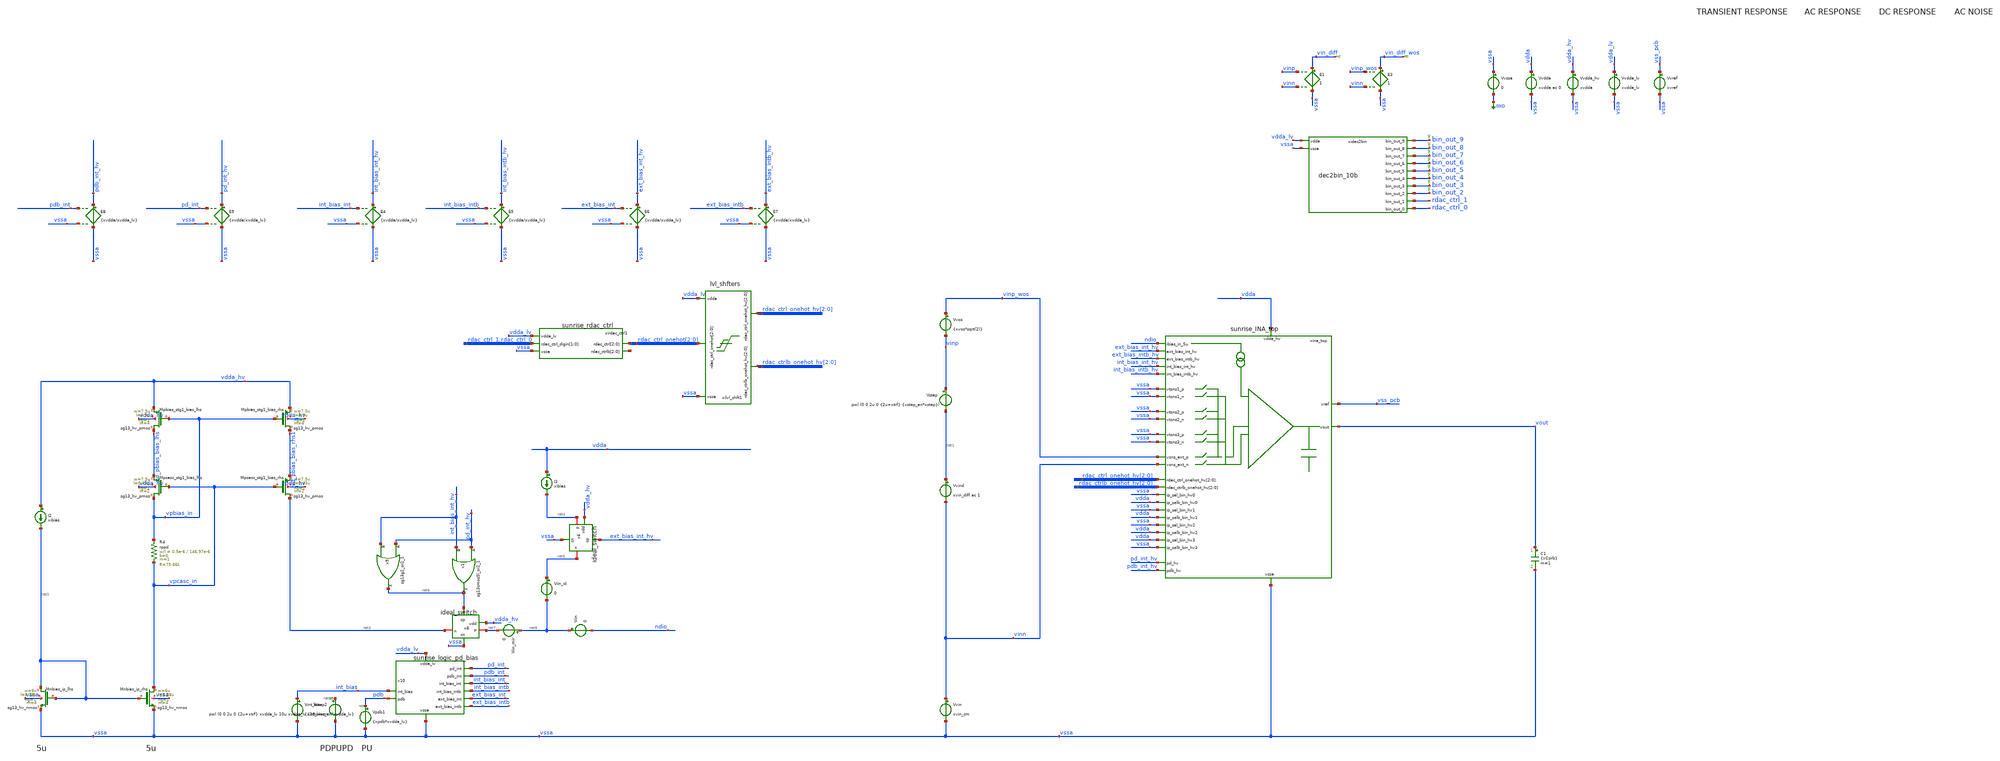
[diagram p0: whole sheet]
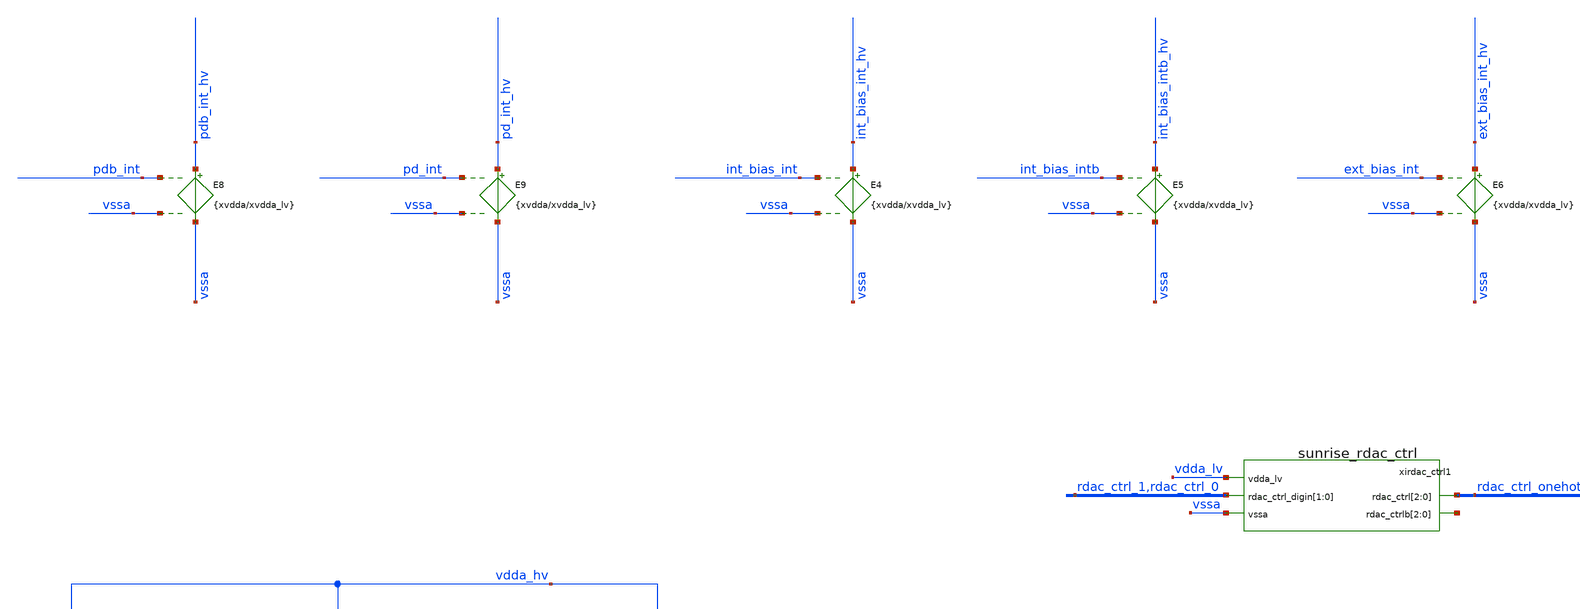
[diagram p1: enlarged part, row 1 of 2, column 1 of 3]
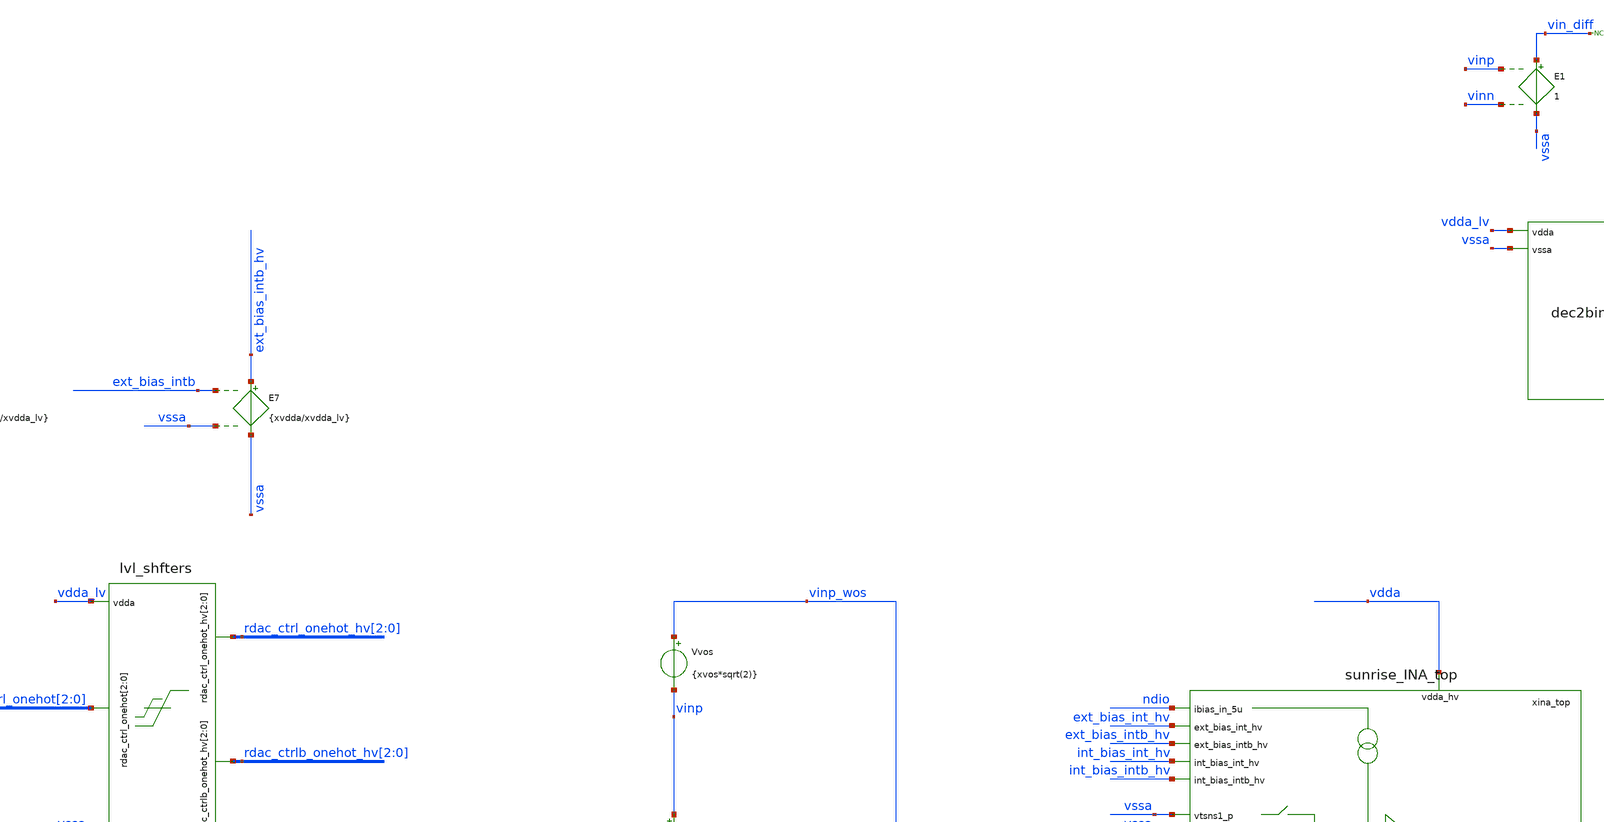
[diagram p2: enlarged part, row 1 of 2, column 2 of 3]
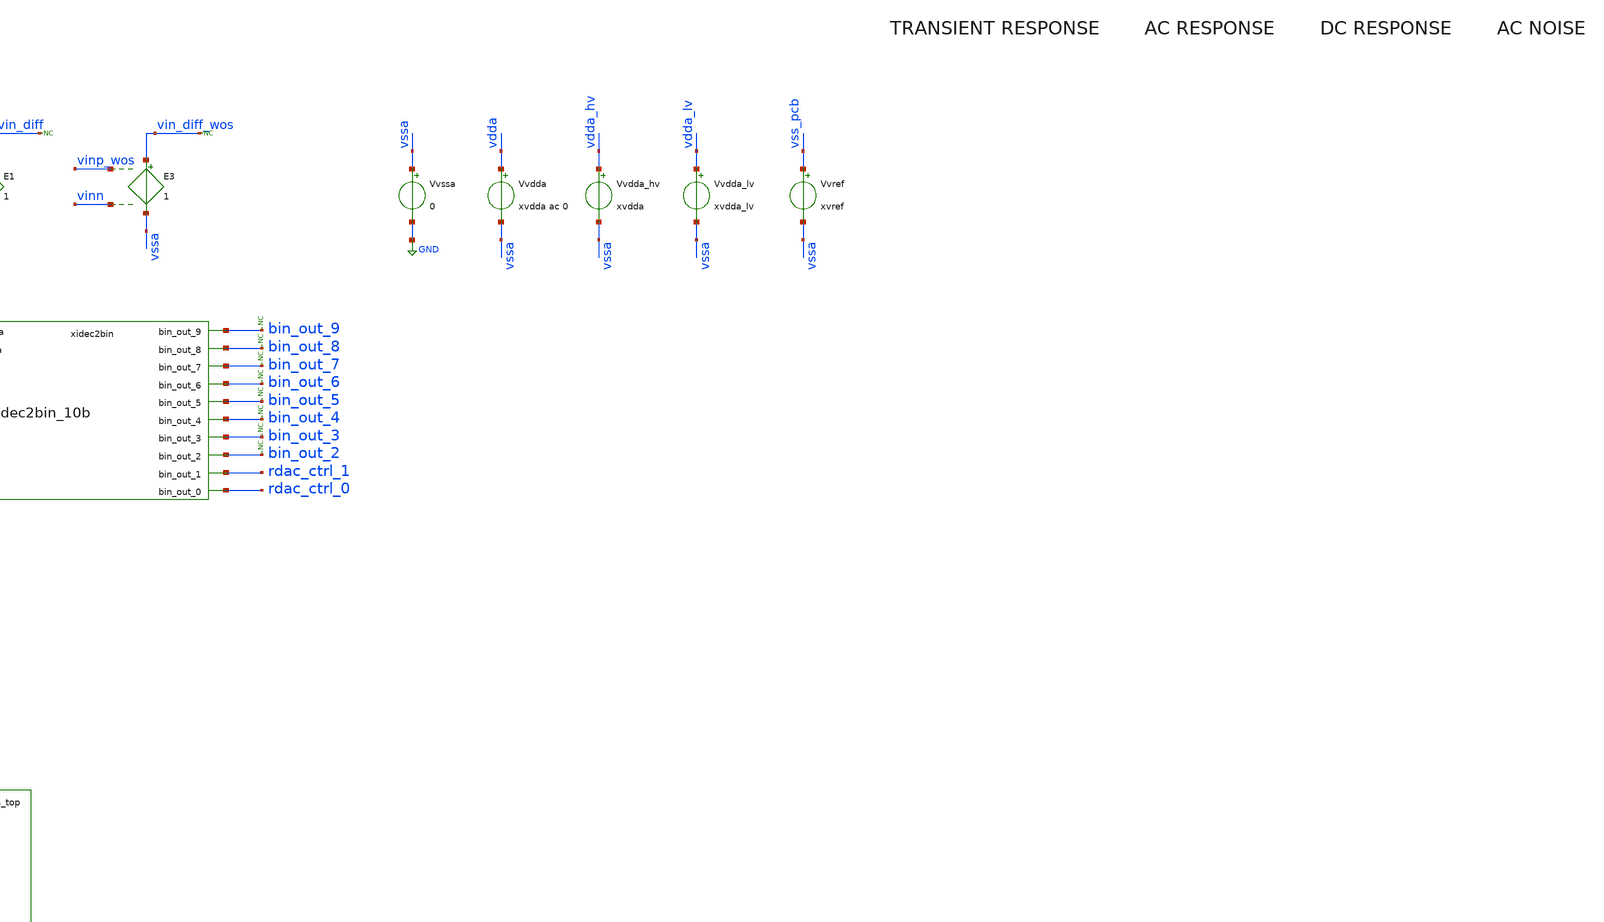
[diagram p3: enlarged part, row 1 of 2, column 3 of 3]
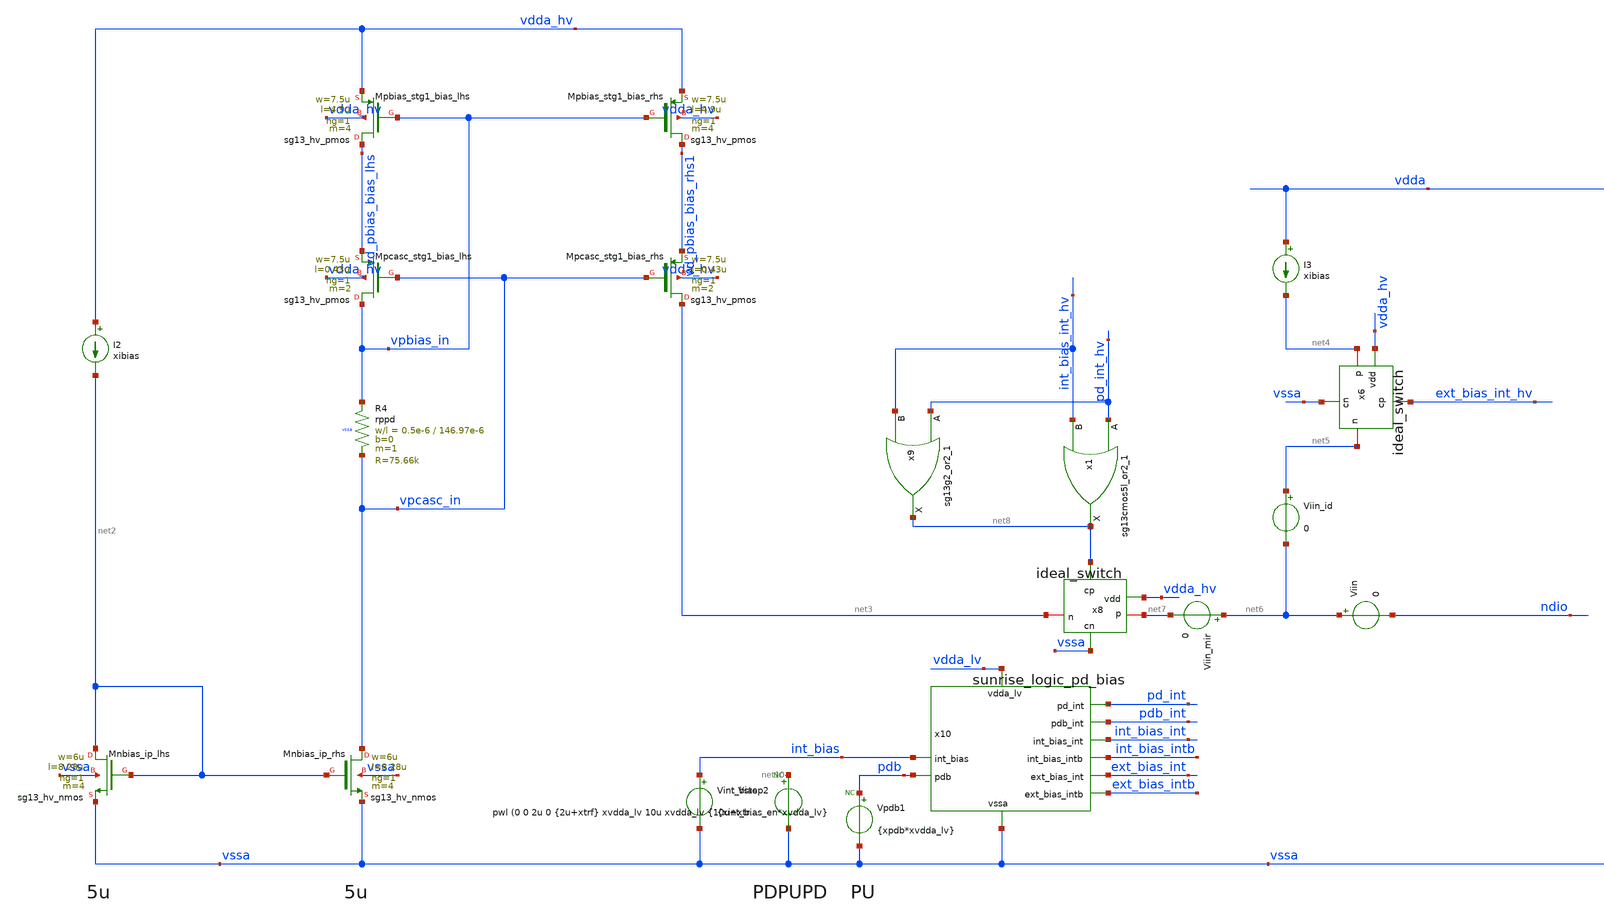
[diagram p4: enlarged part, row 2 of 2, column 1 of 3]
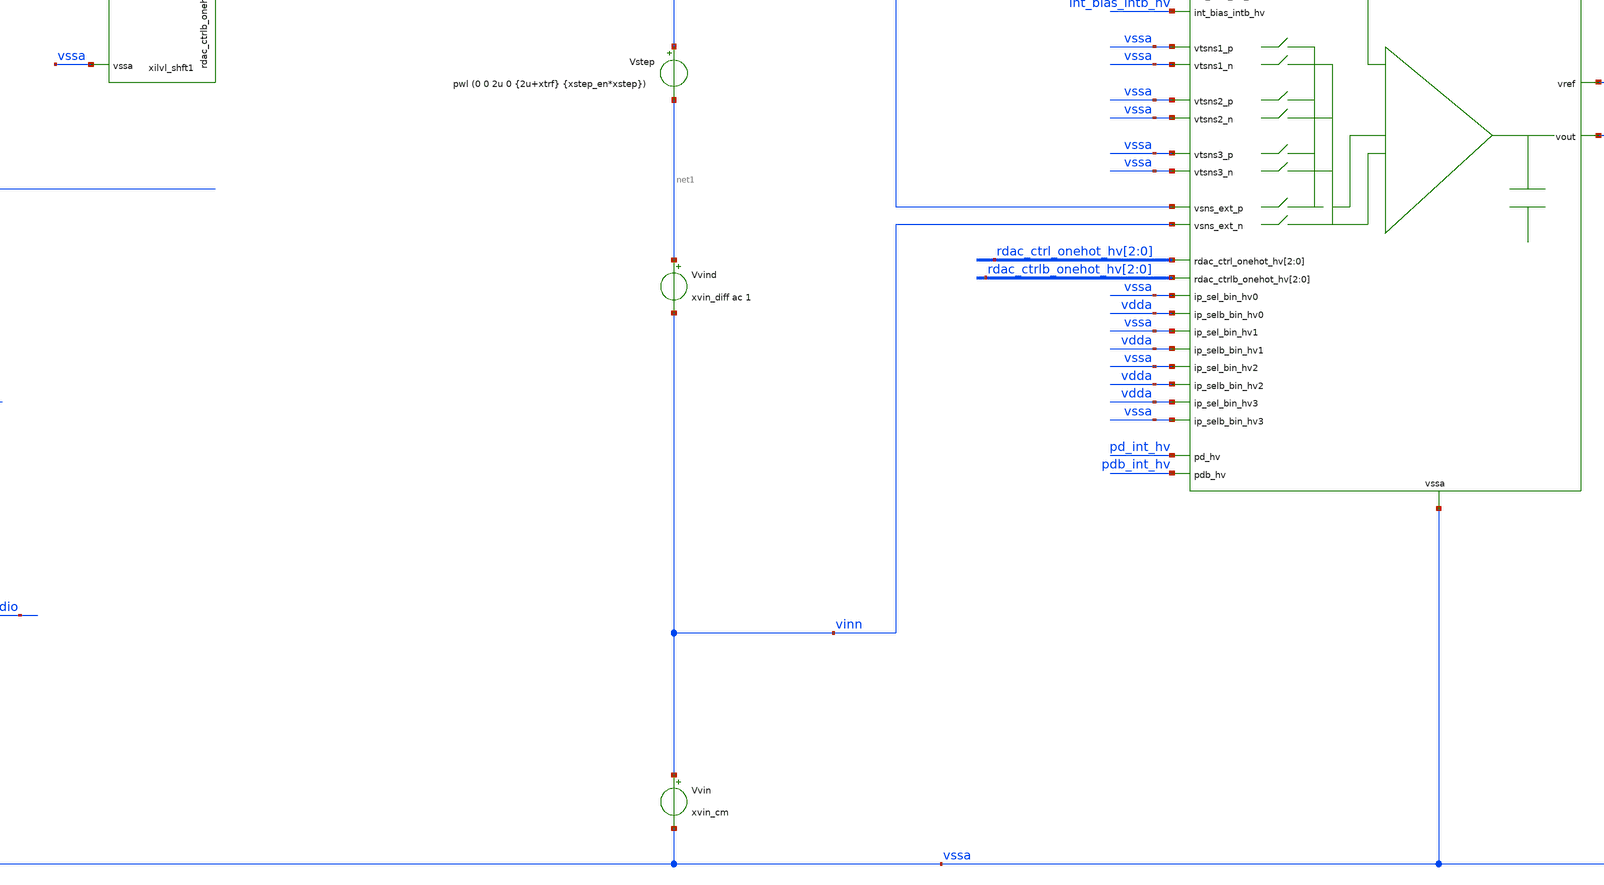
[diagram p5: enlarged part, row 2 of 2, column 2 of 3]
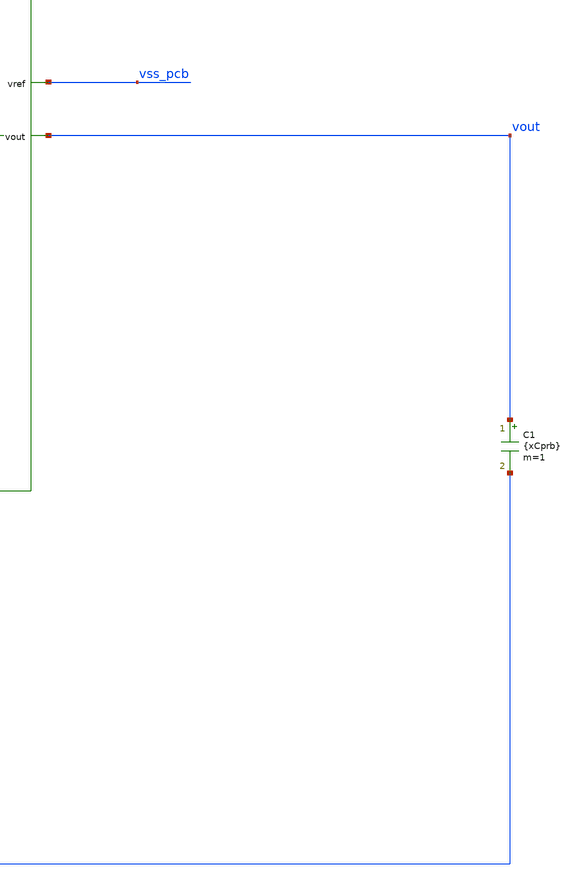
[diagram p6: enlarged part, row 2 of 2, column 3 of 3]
** sch_path: Design_Review_2/INA/Testbench_6_tb_sunrise_ina_top_GE/tb_sunrise_ina_top_GE.sch
**.subckt tb_sunrise_ina_top_GE
Vvssa vssa GND 0
C1 vout vssa {xCprb} m=1
Vvin vinn vssa xvin_cm
Vvind net1 vinn xvin_diff ac 1
E1 vin_diff vssa vinp vinn 1
Vvref vss_pcb vssa xvref
* noconn vin_diff
Vvos vinp_wos vinp {xvos*sqrt(2)}
E3 vin_diff_wos vssa vinp_wos vinn 1
* noconn vin_diff_wos
Vvdda_lv vdda_lv vssa xvdda_lv
xidec2bin bin_out_9 bin_out_8 bin_out_7 bin_out_6 bin_out_5 bin_out_4 bin_out_3 bin_out_2
+ rdac_ctrl_1 rdac_ctrl_0 vdda_lv vssa dec2bin_10b dec_code=dec_code_var
* noconn bin_out_9
* noconn bin_out_8
* noconn bin_out_7
* noconn bin_out_6
* noconn bin_out_5
* noconn bin_out_4
* noconn bin_out_3
* noconn bin_out_2
Vvdda vdda vssa xvdda ac 0
Vstep vinp net1 pwl (0 0 2u 0 {2u+xtrf} {xstep_en*xstep})
xirdac_ctrl1 rdac_ctrl_1 rdac_ctrl_0 rdac_ctrl_onehot[2] rdac_ctrl_onehot[1] rdac_ctrl_onehot[0]
+ vdda_lv vssa net9[2] net9[1] net9[0] sunrise_rdac_ctrl
xilvl_shft1 rdac_ctrl_onehot[2] rdac_ctrl_onehot[1] rdac_ctrl_onehot[0] rdac_ctrlb_onehot_hv[2]
+ rdac_ctrlb_onehot_hv[1] rdac_ctrlb_onehot_hv[0] vssa rdac_ctrl_onehot_hv[2] rdac_ctrl_onehot_hv[1] rdac_ctrl_onehot_hv[0]
+ vdda_lv lvl_shfters
XMnbias_ip_lhs net2 net2 vssa vssa sg13_hv_nmos w=6u l=8.28u ng=1 m=4 mm_ok=1
XMnbias_ip_rhs vpcasc_in net2 vssa vssa sg13_hv_nmos w=6u l=8.28u ng=1 m=4 mm_ok=1
XMpcasc_stg1_bias_lhs vpbias_in vpcasc_in vd_pbias_bias_lhs vdda_hv sg13_hv_pmos w=7.5u l=0.43u ng=1
+ m=2 mm_ok=1
XMpbias_stg1_bias_lhs vd_pbias_bias_lhs vpbias_in vdda_hv vdda_hv sg13_hv_pmos w=7.5u l=4.9u ng=1
+ m=4 mm_ok=1
XMpcasc_stg1_bias_rhs net3 vpcasc_in vd_pbias_bias_rhs1 vdda_hv sg13_hv_pmos w=7.5u l=0.43u ng=1 m=2
+ mm_ok=1
XMpbias_stg1_bias_rhs vd_pbias_bias_rhs1 vpbias_in vdda_hv vdda_hv sg13_hv_pmos w=7.5u l=4.9u ng=1
+ m=4 mm_ok=1
XR4 vpbias_in vpcasc_in vssa rppd w=0.5e-6 l=146.97e-6 m=1 b=0 mm_ok=1
I2 vdda_hv net2 xibias
I3 vdda net4 xibias
Vint_bias int_bias vssa {xint_bias_en*xvdda_lv}
x6 vdda_hv ext_bias_int_hv net4 net5 vssa ideal_switch
x8 vdda_hv net8 net7 net3 vssa ideal_switch
Viin_id net5 net6 0
Viin_mir net6 net7 0
Viin net6 ndio 0
x9 net8 pd_int_hv int_bias_int_hv vdda_hv vssa sg13g2_or2_1
Vstep2 net10 vssa pwl (0 0 2u 0 {2u+xtrf} xvdda_lv 10u xvdda_lv {10u+xtrf} 0)
Vpdb1 pdb vssa {xpdb*xvdda_lv}
* noconn pdb
* noconn #net10
x10 vdda_lv vssa int_bias_intb int_bias int_bias_int pdb ext_bias_intb ext_bias_int pdb_int pd_int
+ sunrise_logic_pd_bias
E4 int_bias_int_hv vssa int_bias_int vssa {xvdda/xvdda_lv}
E5 int_bias_intb_hv vssa int_bias_intb vssa {xvdda/xvdda_lv}
E6 ext_bias_int_hv vssa ext_bias_int vssa {xvdda/xvdda_lv}
E7 ext_bias_intb_hv vssa ext_bias_intb vssa {xvdda/xvdda_lv}
E8 pdb_int_hv vssa pdb_int vssa {xvdda/xvdda_lv}
E9 pd_int_hv vssa pd_int vssa {xvdda/xvdda_lv}
Vvdda_hv vdda_hv vssa xvdda
xina_top vssa vssa vdda vssa vssa ndio ext_bias_int_hv vssa ext_bias_intb_hv int_bias_int_hv vss_pcb
+ int_bias_intb_hv vssa vinp_wos vout vinn rdac_ctrl_onehot_hv[2] rdac_ctrl_onehot_hv[1] rdac_ctrl_onehot_hv[0]
+ rdac_ctrlb_onehot_hv[2] rdac_ctrlb_onehot_hv[1] rdac_ctrlb_onehot_hv[0] vssa vdda pd_int_hv pdb_int_hv vssa vssa vdda vssa
+ vdda vdda vssa sunrise_INA_top
x1 net8 pd_int_hv int_bias_int_hv vdda_hv vssa sg13cmos5l_or2_1
**** begin user architecture code

** opencircuitdesign pdks install
.lib /home/slice/pdk/iHP/IHP-Open-PDK/ihp-sg13g2/libs.tech/ngspice/models/cornerMOSlv.lib mos_tt
.lib /home/slice/pdk/iHP/IHP-Open-PDK/ihp-sg13g2/libs.tech/ngspice/models/cornerMOShv.lib mos_tt
.lib /home/slice/pdk/iHP/IHP-Open-PDK/ihp-sg13g2/libs.tech/ngspice/models/cornerRES.lib res_typ
* SG13G2 STD CELLS
*.include /home/slice/pdk/iHP/IHP-Open-PDK/ihp-sg13g2/libs.ref/sg13g2_stdcell/spice/sg13g2_stdcell.spice
* SG13CMOS5L STD CELLS
.include /home/slice/pdk/iHP/IHP-Open-PDK/ihp-sg13cmos5l/libs.ref/sg13cmos5l_stdcell/spice/sg13cmos5l_stdcell.spice

*.lib /home/slice/pdk/iHP/IHP-Open-PDK/ihp-sg13g2/libs.tech/ngspice/models/cornerMOShv.lib mos_ss
*.lib /home/slice/pdk/iHP/IHP-Open-PDK/ihp-sg13g2/libs.tech/ngspice/models/cornerRES.lib res_wcs
*.lib /home/slice/pdk/iHP/IHP-Open-PDK/ihp-sg13g2/libs.tech/ngspice/models/cornerCAP.lib cap_typ

** PARAMETERS **

* global parameters
.param xvdda = 3.3
.csparam xvdda_hv_var = 'xvdda'
.param xvdda_lv = 1.5
.csparam xvdda_lv_var = 'xvdda_lv'
.param cor_id = 0
.csparam cor_id_var = 'cor_id'
.param xtsim = 40u
.csparam xtsim_var = 'xtsim'
.param xibias = 5u
.param xCfilt = 5p
.param xCprb = 20p
.param xtstep = 100n
.csparam xtstep_var = 'xtstep'
.param xdc_step = 10m
.csparam xdc_step_var = 'xdc_step'
.param xvos = 0m
.param xint_bias_en = 1
* active lo => 0 = pd
.param xpdb = 1
.param xnoise_stg1 = 1
.param xnoise_stg1_ia = 1
.param xnoise_stg1_nia = 1
.param xnoise_stg1_rg = 1
.param xnoise_stg2 = 1
.param xstep = 10m
.param xtrf = 20p
.param xstep_en = 0

* input swing parameters
* Below assumes you want a full input swing
* this is the margin between the supplies which vout can swing to
.param xvmargin = 50m
* max vout
.param xvin_diff_for_vout_max =  (xvdda-(2*xvmargin))/xAv_ina
.csparam xvin_diff_for_vout_max_var = 'xvin_diff_for_vout_max'
* min vout
.param xvin_diff_for_vout_min =  (xvmargin/xAv_ina)
.csparam xvin_diff_for_vout_min_var = 'xvin_diff_for_vout_min'

* set xvin_diff according to desired vout (max or min)
*.param xvin_diff = xvin_diff_for_vout_max

* note on vin_cm: vin_cm_min = max(1V,xAv_ia*vd_max).
* The 1V is due to the NMOS dp and means you cant sense < 1V.
* If you set vcm = xAv_ia*vd_max (assuming this is > 1V),
* you will get a full signal swing at the input (=xvdda/xAv_ina).
* If vcm gets larger, the NIA starts to saturate so dvin needs to be
* be < xvdda/xAv_ina. vin_cm_max simply equals xvdda.
.param xvin_cm = (xAv_ia*((xvdda-(2*xvmargin))/xAv_ina))+xvmargin

* Below assumes you want to pick specific values
*.param xvin_cm = 1.65
.csparam xvin_cm_var = 'xvin_cm'
.param xvin_diff = 10m

* set to the below to measure offset
*.param xvin_diff = 0

* ota model parameters
.param xAv0_dB = 70
.param xAv0 = 10^(xAv0_dB/20)
.param xgmdp = 1m
.param xGBW = 1Meg

* stg1 parameters
* Av = 1 => xRg = 50G, Av = 5 => xRg = 50k, Av = 11 => xRg = 20k, Av = 21 => xRg = 10k
.param xRg= 50k
.param dec_code_var = 1
.csparam xdec_code_var = 'dec_code_var'
* below is to ensure gain error due to xRsw < 1%
*.param xRsw = xRg/100
* below is to manually enter a value for xRsw
.param xRsw = 100
.param xRfb_stg1 = 100k
.param xAv_stg1 = 1+((2*xRfb_stg1)/xRg)
.csparam xAv_stg1_var = 'xAv_stg1'
.param xbeta_stg1 = 1/xAv_stg1
.param lg_stg1 = xAv0*xbeta_stg1
.csparam lg_stg1_var = 'lg_stg1'
.param xAv_ia = xRfb_stg1/xRg

* stg2 parameters
*.param xvref = 3.3/2
.param xvref = 50m
.param xRin_stg2 = 10k
.param xRfb_stg2 = 10k
.param xAv_stg2 = xRfb_stg2/xRin_stg2
.csparam xAv_stg2_var = 'xAv_stg2'
.param xbeta_stg2 = xRin_stg2/(xRin_stg2+xRfb_stg2)
.param lg_stg2 = xAv0*xbeta_stg2
.csparam lg_stg2_var = 'lg_stg2'

* total ina gain parameter
.param xAv_ina = xAv_stg1*xAv_stg2
.csparam xAv_ina_var = 'xAv_ina'

.temp 27

* vlogA instantiations
.model OTA_vcvs OTA_vcvs
.model ideal_sw ideal_sw
.model dec2bin_10b dec2bin_10b

.include tb_sunrise_ina_top_GE.save

* below line needs to be included if running ac noise analysys
.save all


*.option savecurrents

*.save onoise* inoise* frequency
.save i(v.xstb.Vi) v(xstb.x) v(av)
.save v(vinp) v(vinn) v(vinp_wos) v(vin_diff) v(vin_diff_wos) v(vfb_ni) v(vfb_i) v(vih) v(vil) v(vip_stg2) v(vin_stg2) v(vin_stg2_diff) v(vout)
.save v(vdda) v(vdda_lv) v(vssa) v(vss_pcb) v(ibias1) v(ibias2) v(ibias3) v(vfb_ni2) v(vfb_i2) v(rdac_ctrl_1) v(rdac_ctrl_0)
.save v(xirdac.xirdac_ctrl.rdac_ctrl_int[0]) v(xirdac.xirdac_ctrl.rdac_ctrlb_int[0]) v(xirdac.xirdac_ctrl.rdac_ctrl_int[1]) v(xirdac.xirdac_ctrl.rdac_ctrlb_int[1]) v(xirdac.rdac_ctrl_onehot[2]) v(xirdac.rdac_ctrl_onehot[1]) v(xirdac.rdac_ctrl_onehot[0]) v(xirdac.rdac_ctrl_onehot_hv[2]) v(xirdac.rdac_ctrl_onehot_hv[1]) v(xirdac.rdac_ctrl_onehot_hv[0]) v(xirdac.rdac_ctrlb_onehot_hv[2]) v(xirdac.rdac_ctrlb_onehot_hv[1]) v(xirdac.rdac_ctrlb_onehot_hv[0])



.control

pre_osdi OTA_vcvs.osdi
pre_osdi ideal_sw.osdi
pre_osdi dec2bin_10b.osdi

 * commercial temperature range
 *set xTj = ( 0 10 20 30 40 50 60 70 )
 * industrial temperature range
 *set xTj = ( -40 -30 -20 -10 0 10 20 30 40 50 60 70 85 )
 * military temperature range
 *set xTj = ( -55 -40 -30 -20 -10 0 10 20 30 40 50 60 70 80 90 100 110 125 )
 * automotive temperature range
 *set xTj = ( -40 -30 -20 -10 0 10 20 30 40 50 60 70 80 90 100 110 120 130 140 150 )
 set xTj = ( 27 )

  foreach xTj_var $xTj

  let Tj_meas = $xTj_var

  echo temperature is "$&Tj_meas"

  *echo "$&Tj_meas" >> Temp_measures.txt

  set temp = $xTj_var
  echo $temp

** 1. DC ANALYSIS **
  echo xvin_diff_for_vout_max_var = "$&xvin_diff_for_vout_max_var"
  echo xvin_cm_var = "$&xvin_cm_var"

  dc Vvind 0 $&xvin_diff_for_vout_max_var $&xdc_step_var
  * below variable outputted for octave plot.
  * Note: Anytime a new variable gets added the octave script needs to be updated.
  echo --
  let numsteps4octave = ($&xvin_diff_for_vout_max_var/$&xdc_step_var)+1
  print numsteps4octave
  echo --
  remzerovec
  set filetype=binary
  write tb_sunrise_ina_dc.raw
  set filetype=ascii
  write tb_sunrise_ina_dc_ascii.raw

** 1. DC MEASURES **

  let x1 = xvin_cm_var+1m
  echo x1 = "$&x1"
  meas DC y1 FIND v(vout) WHEN v(vinp)=$&x1 CROSS=1
  let x2 = xvin_cm_var+xvin_diff_for_vout_max_var-10m
  echo x2 = "$&x2"
  meas DC y2 FIND v(vout) WHEN v(vinp)=$&x2 CROSS=1

  let gain = (y2-y1)/(x2-x1)
  echo Av_re = "$&gain"
  echo Av_id = "$&xAv_ina_var"
  let gain_error = ((gain-xAv_ina_var)/xAv_ina_var)*100
  echo gain_error = "$&gain_error"

  * 1.0 Global parameters:
  echo cor_id = "$&cor_id_var"
  echo "$&cor_id_var" > ge.txt
  echo --
  echo temp = "$temp"
  echo "$temp" >> ge.txt
  echo --
  echo vdda_hv = "$&xvdda_hv_var"
  echo "$&xvdda_hv_var" >> ge.txt
  echo --
  echo vdda_lv = "$&xvdda_lv_var"
  echo "$&xvdda_lv_var" >> ge.txt
  echo --
  echo "$&gain_error" >> ge.txt
  echo --

  end

  setplot
*quit 0
.endc




**** end user architecture code
**.ends
.GLOBAL GND
.end
